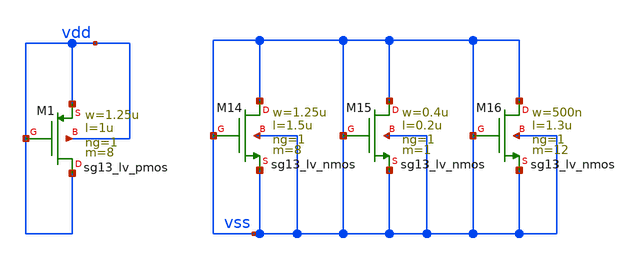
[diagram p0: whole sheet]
** sch_path: v2_feature_extr/neuron_n_ADC_nocap_dummy_dev.sch
**.subckt neuron_n_ADC_nocap_dummy_dev
XM1 vdd vdd vdd vdd sg13_lv_pmos w=1.25u l=1u ng=1 m=8 mm_ok=1
XM14 vss vss vss vss sg13_lv_nmos w=1.25u l=1.5u ng=1 m=8 mm_ok=1
XM15 vss vss vss vss sg13_lv_nmos w=0.4u l=0.2u ng=1 m=1 mm_ok=1
XM16 vss vss vss vss sg13_lv_nmos w=500n l=1.3u ng=1 m=12 mm_ok=1
**.ends
.end
